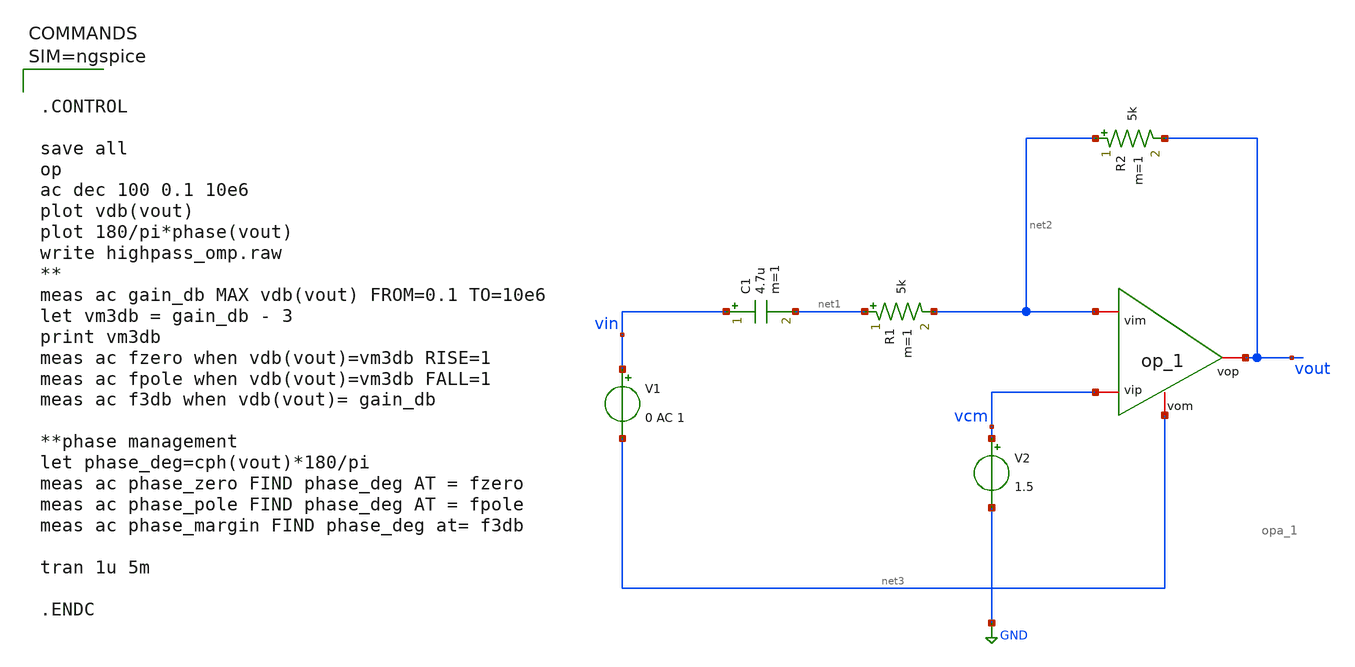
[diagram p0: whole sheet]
** sch_path: work/xschem/highpass_omp.sch
**.subckt highpass_omp
C1 vin net1 4.7u m=1
R1 net1 net2 5k m=1
V1 vin net3 0 AC 1
V2 vcm GND 1.5
R2 net2 vout 5k m=1
x1 vout vcm net2 net3 opa_1
**** begin user architecture code



.CONTROL

save all
op
ac dec 100 0.1 10e6
plot vdb(vout)
plot 180/pi*phase(vout)
write highpass_omp.raw
**
meas ac gain_db MAX vdb(vout) FROM=0.1 TO=10e6
let vm3db = gain_db - 3
print vm3db
meas ac fzero when vdb(vout)=vm3db RISE=1
meas ac fpole when vdb(vout)=vm3db FALL=1
meas ac f3db when vdb(vout)= gain_db

**phase management
let phase_deg=cph(vout)*180/pi
meas ac phase_zero FIND phase_deg AT = fzero
meas ac phase_pole FIND phase_deg AT = fpole
meas ac phase_margin FIND phase_deg at= f3db

tran 1u 5m

.ENDC



**** end user architecture code
**.ends
.GLOBAL GND
.end
